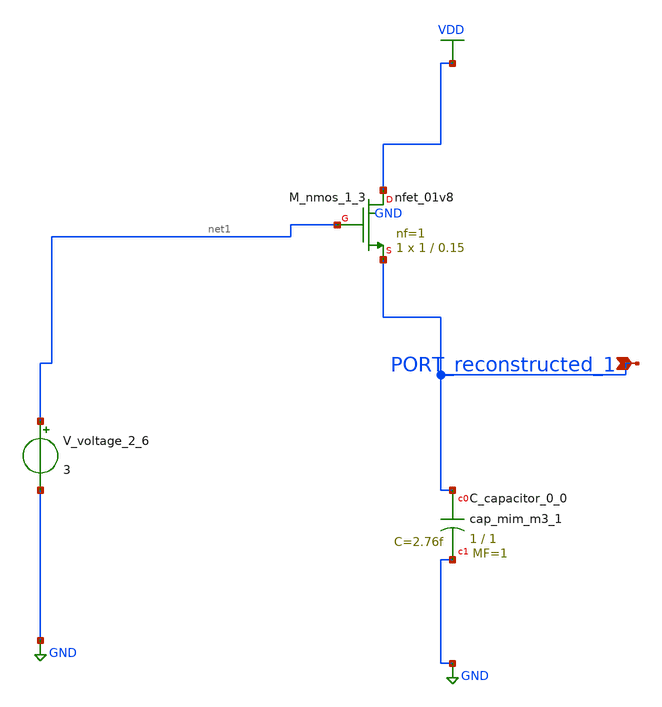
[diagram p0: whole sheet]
** sch_path: schematics/AMSNet/49.sch
**.subckt 49 PORT_reconstructed_1
*.ipin PORT_reconstructed_1
XC_capacitor_0_0 PORT_reconstructed_1 GND sky130_fd_pr__cap_mim_m3_1 W=1 L=1 MF=1 m=1
XM_nmos_1_3 VDD net1 PORT_reconstructed_1 GND sky130_fd_pr__nfet_01v8 L=0.15 W=1 nf=1 ad='int((1 + 1)/2) * 1 / 1 * 0.29'
+ as='int((1 + 2)/2) * 1 / 1 * 0.29' pd='2*int((1 + 1)/2) * (1 / 1 + 0.29)' ps='2*int((1 + 2)/2) * (1 / 1 + 0.29)'
+ nrd='0.29 / 1 ' nrs='0.29 / 1 ' sa=0 sb=0 sd=0 mult=1 m=1
V_voltage_2_6 net1 GND 3
**.ends
.GLOBAL GND
.GLOBAL VDD
.end
